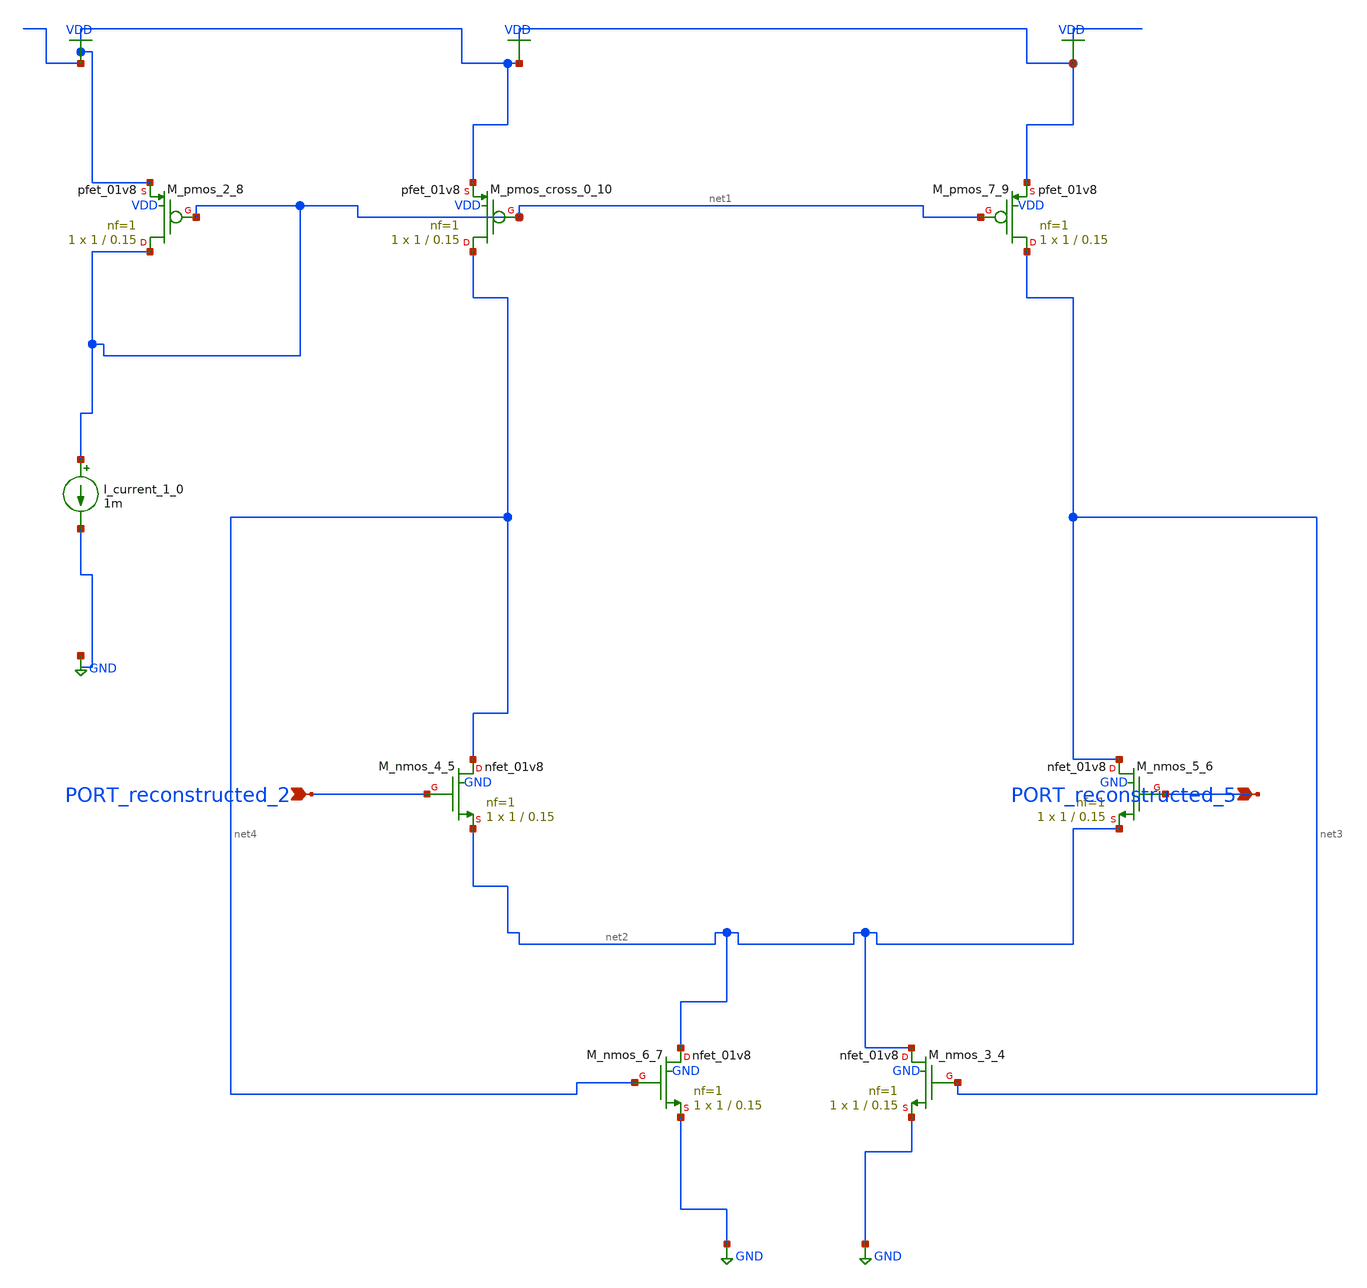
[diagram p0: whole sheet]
** sch_path: schematics/AMSNet/676.sch
**.subckt 676 PORT_reconstructed_5 PORT_reconstructed_2
*.ipin PORT_reconstructed_5
*.ipin PORT_reconstructed_2
I_current_1_0 net1 GND 1m
XM_nmos_3_4 net2 net3 GND GND sky130_fd_pr__nfet_01v8 L=0.15 W=1 nf=1 ad='int((1 + 1)/2) * 1 / 1 * 0.29'
+ as='int((1 + 2)/2) * 1 / 1 * 0.29' pd='2*int((1 + 1)/2) * (1 / 1 + 0.29)' ps='2*int((1 + 2)/2) * (1 / 1 + 0.29)'
+ nrd='0.29 / 1 ' nrs='0.29 / 1 ' sa=0 sb=0 sd=0 mult=1 m=1
XM_nmos_4_5 net4 PORT_reconstructed_2 net2 GND sky130_fd_pr__nfet_01v8 L=0.15 W=1 nf=1 ad='int((1 + 1)/2) * 1 / 1 * 0.29'
+ as='int((1 + 2)/2) * 1 / 1 * 0.29' pd='2*int((1 + 1)/2) * (1 / 1 + 0.29)' ps='2*int((1 + 2)/2) * (1 / 1 + 0.29)'
+ nrd='0.29 / 1 ' nrs='0.29 / 1 ' sa=0 sb=0 sd=0 mult=1 m=1
XM_nmos_5_6 net3 PORT_reconstructed_5 net2 GND sky130_fd_pr__nfet_01v8 L=0.15 W=1 nf=1 ad='int((1 + 1)/2) * 1 / 1 * 0.29'
+ as='int((1 + 2)/2) * 1 / 1 * 0.29' pd='2*int((1 + 1)/2) * (1 / 1 + 0.29)' ps='2*int((1 + 2)/2) * (1 / 1 + 0.29)'
+ nrd='0.29 / 1 ' nrs='0.29 / 1 ' sa=0 sb=0 sd=0 mult=1 m=1
XM_nmos_6_7 net2 net4 GND GND sky130_fd_pr__nfet_01v8 L=0.15 W=1 nf=1 ad='int((1 + 1)/2) * 1 / 1 * 0.29'
+ as='int((1 + 2)/2) * 1 / 1 * 0.29' pd='2*int((1 + 1)/2) * (1 / 1 + 0.29)' ps='2*int((1 + 2)/2) * (1 / 1 + 0.29)'
+ nrd='0.29 / 1 ' nrs='0.29 / 1 ' sa=0 sb=0 sd=0 mult=1 m=1
XM_pmos_2_8 net1 net1 VDD VDD sky130_fd_pr__pfet_01v8 L=0.15 W=1 nf=1 ad='int((1 + 1)/2) * 1 / 1 * 0.29'
+ as='int((1 + 2)/2) * 1 / 1 * 0.29' pd='2*int((1 + 1)/2) * (1 / 1 + 0.29)' ps='2*int((1 + 2)/2) * (1 / 1 + 0.29)'
+ nrd='0.29 / 1 ' nrs='0.29 / 1 ' sa=0 sb=0 sd=0 mult=1 m=1
XM_pmos_7_9 net3 net1 VDD VDD sky130_fd_pr__pfet_01v8 L=0.15 W=1 nf=1 ad='int((1 + 1)/2) * 1 / 1 * 0.29'
+ as='int((1 + 2)/2) * 1 / 1 * 0.29' pd='2*int((1 + 1)/2) * (1 / 1 + 0.29)' ps='2*int((1 + 2)/2) * (1 / 1 + 0.29)'
+ nrd='0.29 / 1 ' nrs='0.29 / 1 ' sa=0 sb=0 sd=0 mult=1 m=1
XM_pmos_cross_0_10 net4 net1 VDD VDD sky130_fd_pr__pfet_01v8 L=0.15 W=1 nf=1 ad='int((1 + 1)/2) * 1 / 1 * 0.29'
+ as='int((1 + 2)/2) * 1 / 1 * 0.29' pd='2*int((1 + 1)/2) * (1 / 1 + 0.29)' ps='2*int((1 + 2)/2) * (1 / 1 + 0.29)'
+ nrd='0.29 / 1 ' nrs='0.29 / 1 ' sa=0 sb=0 sd=0 mult=1 m=1
**.ends
.GLOBAL GND
.GLOBAL VDD
.end
